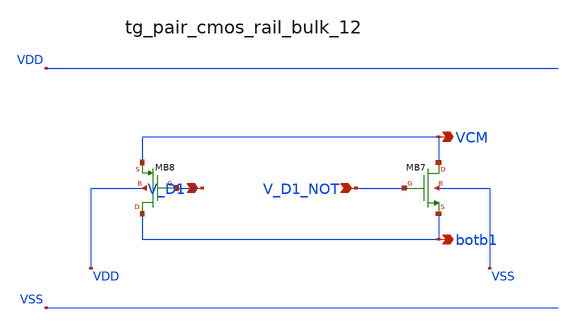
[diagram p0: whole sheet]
** sch_path: analog-db/raw/ia_005_hsu_pga_ideal/hier/blocks/tg_pair_cmos_rail_bulk_12.sch
**.subckt tg_pair_cmos_rail_bulk_12 V_D1 V_D1_NOT VCM botb1
*.ipin V_D1
*.ipin V_D1_NOT
*.opin VCM
*.opin botb1
XMB7 VCM V_D1_NOT botb1 VSS sg13_lv_nmos w=x_dut_xmb7_w l=x_dut_xmb7_l ng=1 m=x_dut_xmb7_m
XMB8 botb1 V_D1 VCM VDD sg13_lv_pmos w=x_dut_xmb8_w l=x_dut_xmb8_l ng=1 m=x_dut_xmb8_m
**.ends
.end
